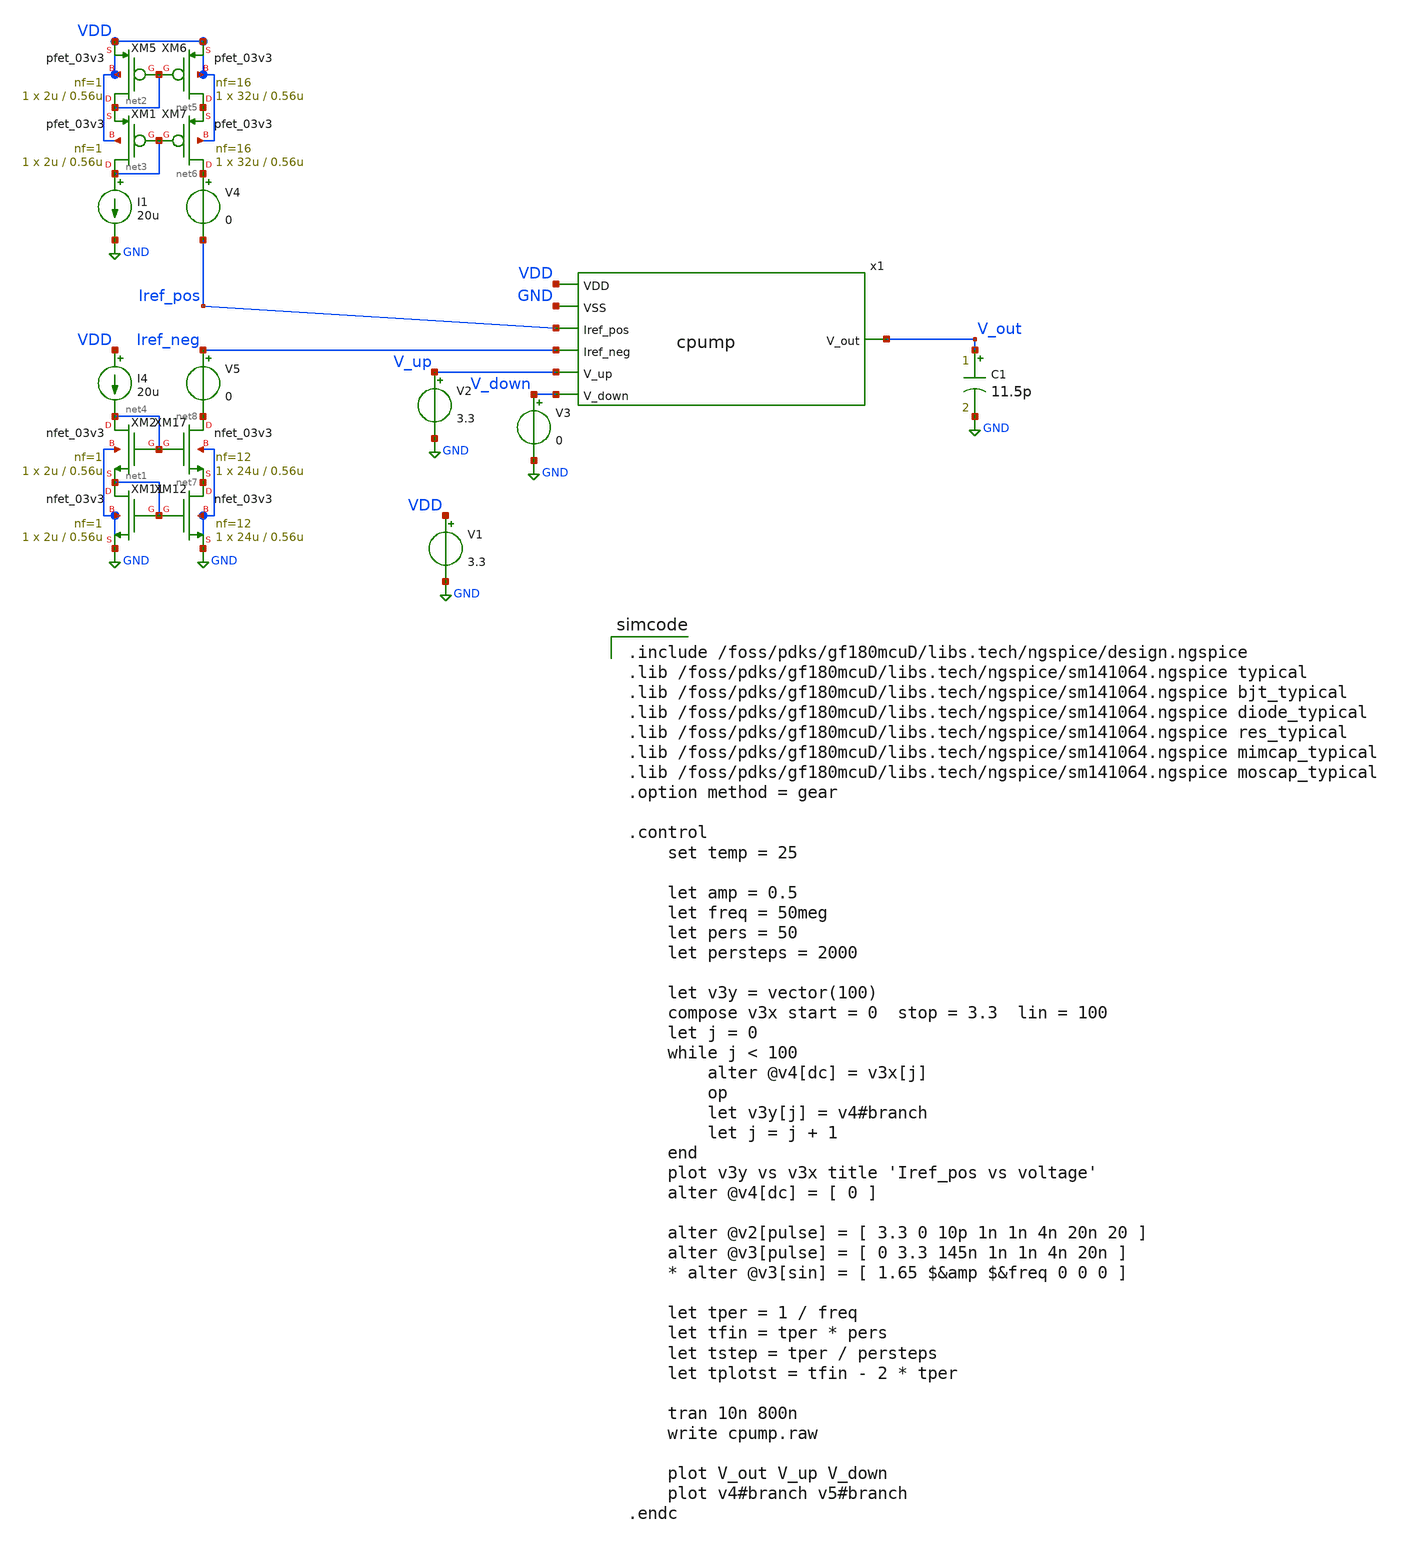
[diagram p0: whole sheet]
** sch_path: rha-vga-pll-blocks/blocks/pll/cpump_tb.sch
**.subckt cpump_tb
x1 Iref_pos VDD V_up V_out V_down GND Iref_neg cpump
V1 VDD GND 3.3
V2 V_up GND 3.3
V3 V_down GND 0
I1 net3 GND 20u
XM5 net2 net2 VDD VDD pfet_03v3 L=0.56u W=2u nf=1 ad='int((nf+1)/2) * W/nf * 0.18u' as='int((nf+2)/2) * W/nf * 0.18u'
+ pd='2*int((nf+1)/2) * (W/nf + 0.18u)' ps='2*int((nf+2)/2) * (W/nf + 0.18u)' nrd='0.18u / W' nrs='0.18u / W'
+ sa=0 sb=0 sd=0 m=1
XM6 net5 net2 VDD VDD pfet_03v3 L=0.56u W=32u nf=16 ad='int((nf+1)/2) * W/nf * 0.18u' as='int((nf+2)/2) * W/nf * 0.18u'
+ pd='2*int((nf+1)/2) * (W/nf + 0.18u)' ps='2*int((nf+2)/2) * (W/nf + 0.18u)' nrd='0.18u / W' nrs='0.18u / W'
+ sa=0 sb=0 sd=0 m=1
XM7 net6 net3 net5 VDD pfet_03v3 L=0.56u W=32u nf=16 ad='int((nf+1)/2) * W/nf * 0.18u' as='int((nf+2)/2) * W/nf * 0.18u'
+ pd='2*int((nf+1)/2) * (W/nf + 0.18u)' ps='2*int((nf+2)/2) * (W/nf + 0.18u)' nrd='0.18u / W' nrs='0.18u / W'
+ sa=0 sb=0 sd=0 m=1
V4 net6 Iref_pos 0
I4 VDD net4 20u
XM11 net1 net1 GND GND nfet_03v3 L=0.56u W=2u nf=1 ad='int((nf+1)/2) * W/nf * 0.18u' as='int((nf+2)/2) * W/nf * 0.18u'
+ pd='2*int((nf+1)/2) * (W/nf + 0.18u)' ps='2*int((nf+2)/2) * (W/nf + 0.18u)' nrd='0.18u / W' nrs='0.18u / W'
+ sa=0 sb=0 sd=0 m=1
XM12 net7 net1 GND GND nfet_03v3 L=0.56u W=24u nf=12 ad='int((nf+1)/2) * W/nf * 0.18u' as='int((nf+2)/2) * W/nf * 0.18u'
+ pd='2*int((nf+1)/2) * (W/nf + 0.18u)' ps='2*int((nf+2)/2) * (W/nf + 0.18u)' nrd='0.18u / W' nrs='0.18u / W'
+ sa=0 sb=0 sd=0 m=1
XM17 net8 net4 net7 GND nfet_03v3 L=0.56u W=24u nf=12 ad='int((nf+1)/2) * W/nf * 0.18u' as='int((nf+2)/2) * W/nf * 0.18u'
+ pd='2*int((nf+1)/2) * (W/nf + 0.18u)' ps='2*int((nf+2)/2) * (W/nf + 0.18u)' nrd='0.18u / W' nrs='0.18u / W'
+ sa=0 sb=0 sd=0 m=1
V5 Iref_neg net8 0
C1 V_out GND 11.5p m=1
XM1 net3 net3 net2 VDD pfet_03v3 L=0.56u W=2u nf=1 ad='int((nf+1)/2) * W/nf * 0.18u' as='int((nf+2)/2) * W/nf * 0.18u'
+ pd='2*int((nf+1)/2) * (W/nf + 0.18u)' ps='2*int((nf+2)/2) * (W/nf + 0.18u)' nrd='0.18u / W' nrs='0.18u / W'
+ sa=0 sb=0 sd=0 m=1
XM2 net4 net4 net1 GND nfet_03v3 L=0.56u W=2u nf=1 ad='int((nf+1)/2) * W/nf * 0.18u' as='int((nf+2)/2) * W/nf * 0.18u'
+ pd='2*int((nf+1)/2) * (W/nf + 0.18u)' ps='2*int((nf+2)/2) * (W/nf + 0.18u)' nrd='0.18u / W' nrs='0.18u / W'
+ sa=0 sb=0 sd=0 m=1
**** begin user architecture code

.include /foss/pdks/gf180mcuD/libs.tech/ngspice/design.ngspice
.lib /foss/pdks/gf180mcuD/libs.tech/ngspice/sm141064.ngspice typical
.lib /foss/pdks/gf180mcuD/libs.tech/ngspice/sm141064.ngspice bjt_typical
.lib /foss/pdks/gf180mcuD/libs.tech/ngspice/sm141064.ngspice diode_typical
.lib /foss/pdks/gf180mcuD/libs.tech/ngspice/sm141064.ngspice res_typical
.lib /foss/pdks/gf180mcuD/libs.tech/ngspice/sm141064.ngspice mimcap_typical
.lib /foss/pdks/gf180mcuD/libs.tech/ngspice/sm141064.ngspice moscap_typical
.option method = gear

.control
    set temp = 25

    let amp = 0.5
    let freq = 50meg
    let pers = 50
    let persteps = 2000

    let v3y = vector(100)
    compose v3x start = 0  stop = 3.3  lin = 100
    let j = 0
    while j < 100
        alter @v4[dc] = v3x[j]
        op
        let v3y[j] = v4#branch
        let j = j + 1
    end
    plot v3y vs v3x title 'Iref_pos vs voltage'
    alter @v4[dc] = [ 0 ]

    alter @v2[pulse] = [ 3.3 0 10p 1n 1n 4n 20n 20 ]
    alter @v3[pulse] = [ 0 3.3 145n 1n 1n 4n 20n ]
    * alter @v3[sin] = [ 1.65 $&amp $&freq 0 0 0 ]

    let tper = 1 / freq
    let tfin = tper * pers
    let tstep = tper / persteps
    let tplotst = tfin - 2 * tper

    tran 10n 800n
    write cpump.raw

    plot V_out V_up V_down
    plot v4#branch v5#branch
.endc


**** end user architecture code
**.ends

* expanding   symbol:  blocks/pll/cpump.sym # of pins=7
** sym_path: blocks/pll/cpump.sym
** sch_path: blocks/pll/cpump.sch
.subckt cpump Iref_pos VDD V_up V_out V_down VSS Iref_neg
*.ipin Iref_pos
*.ipin Iref_neg
*.ipin V_up
*.ipin V_down
*.iopin VDD
*.iopin VSS
*.opin V_out
XM2 V_out V_down Iref_neg VSS nfet_03v3 L=0.56u W=19.2u nf=4 ad='int((nf+1)/2) * W/nf * 0.18u' as='int((nf+2)/2) * W/nf * 0.18u'
+ pd='2*int((nf+1)/2) * (W/nf + 0.18u)' ps='2*int((nf+2)/2) * (W/nf + 0.18u)' nrd='0.18u / W' nrs='0.18u / W'
+ sa=0 sb=0 sd=0 m=1
XR1 net1 V_out VSS ppolyf_u_1k r_width=2e-6 r_length=32e-6 m=1
XM1 V_out V_up Iref_pos VDD pfet_03v3 L=0.56u W=19.2u nf=4 ad='int((nf+1)/2) * W/nf * 0.18u' as='int((nf+2)/2) * W/nf * 0.18u'
+ pd='2*int((nf+1)/2) * (W/nf + 0.18u)' ps='2*int((nf+2)/2) * (W/nf + 0.18u)' nrd='0.18u / W' nrs='0.18u / W'
+ sa=0 sb=0 sd=0 m=1
XC2 net1 VSS cap_mim_2f0_m4m5_noshield c_width=35e-6 c_length=35e-6 m=1
.ends

.GLOBAL GND
.end
